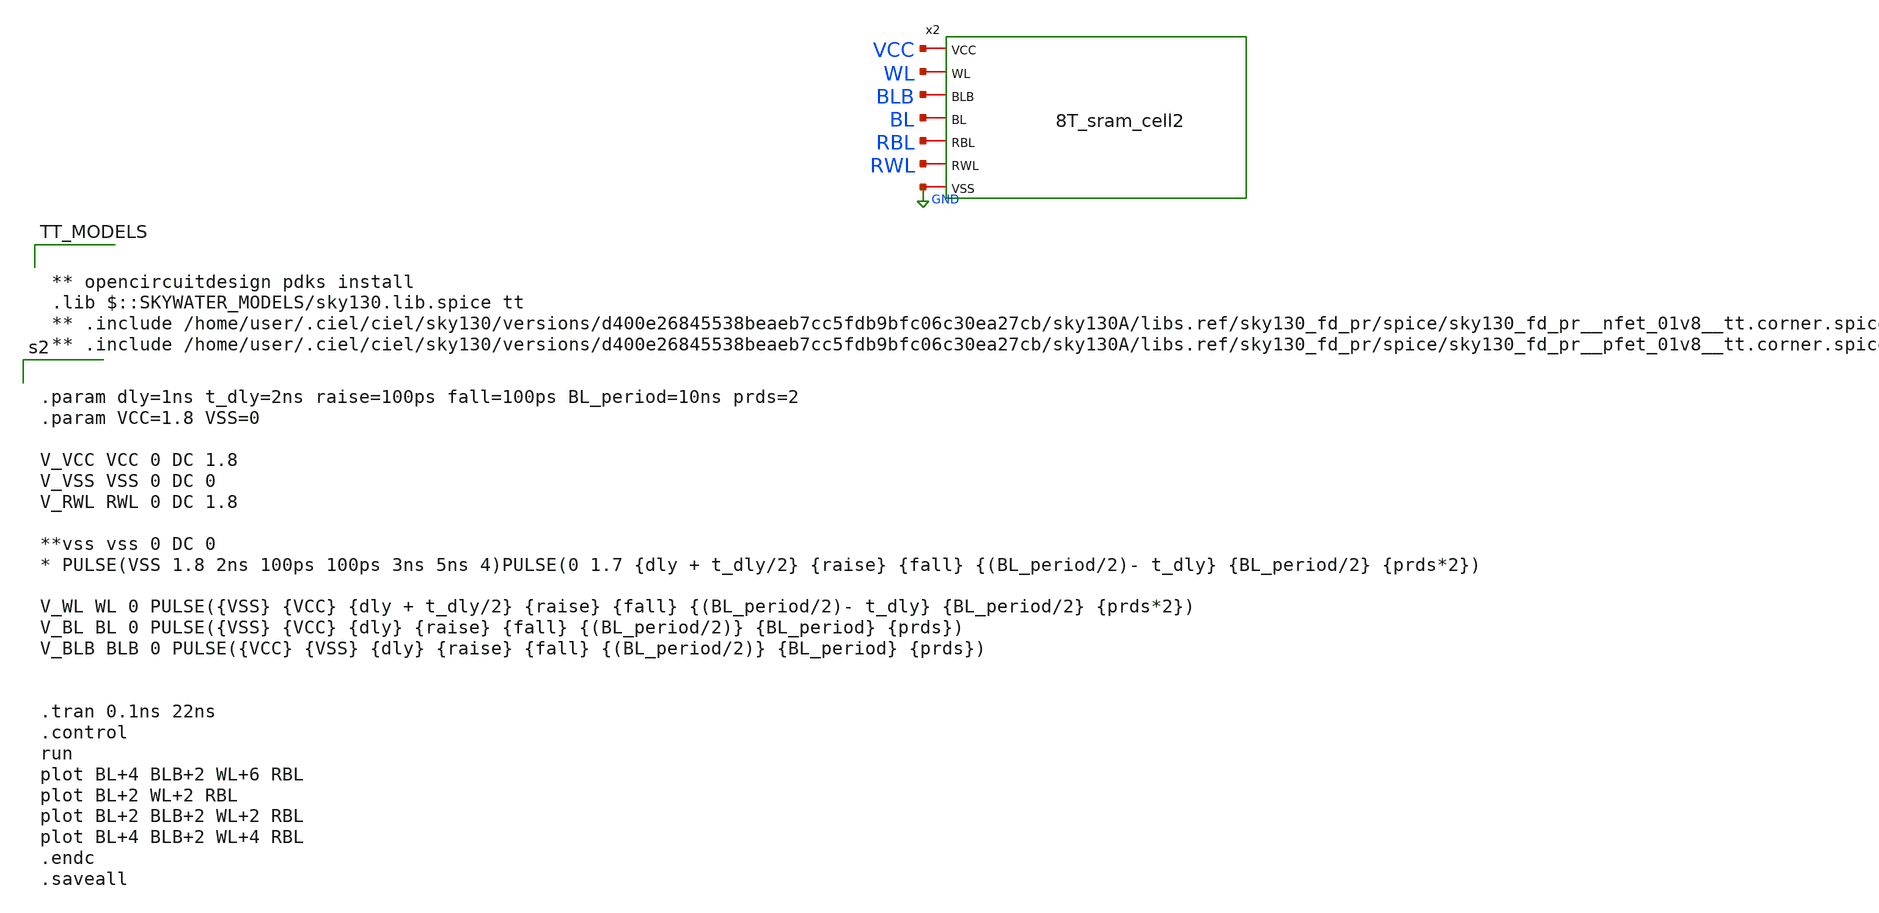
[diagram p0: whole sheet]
** sch_path: 8T_sram_array_test.sch
**.subckt 8T_sram_array_test
x2 VCC WL BLB BL RBL RWL GND 8T_sram_cell2
**** begin user architecture code


.param dly=1ns t_dly=2ns raise=100ps fall=100ps BL_period=10ns prds=2
.param VCC=1.8 VSS=0

V_VCC VCC 0 DC 1.8
V_VSS VSS 0 DC 0
V_RWL RWL 0 DC 1.8

**vss vss 0 DC 0
* PULSE(VSS 1.8 2ns 100ps 100ps 3ns 5ns 4)PULSE(0 1.7 {dly + t_dly/2} {raise} {fall} {(BL_period/2)- t_dly}
*+ {BL_period/2} {prds*2})

V_WL WL 0 PULSE({VSS} {VCC} {dly + t_dly/2} {raise} {fall} {(BL_period/2)- t_dly} {BL_period/2} {prds*2})
V_BL BL 0 PULSE({VSS} {VCC} {dly} {raise} {fall} {(BL_period/2)} {BL_period} {prds})
V_BLB BLB 0 PULSE({VCC} {VSS} {dly} {raise} {fall} {(BL_period/2)} {BL_period} {prds})


.tran 0.1ns 22ns
.control
run
plot BL+4 BLB+2 WL+6 RBL
plot BL+2 WL+2 RBL
plot BL+2 BLB+2 WL+2 RBL
plot BL+4 BLB+2 WL+4 RBL
.endc
.saveall




** opencircuitdesign pdks install
.lib $::SKYWATER_MODELS/sky130.lib.spice tt
** .include
*+ /home/user/.ciel/ciel/sky130/versions/d400e26845538beaeb7cc5fdb9bfc06c30ea27cb/sky130A/libs.ref/sky130_fd_pr/spice/sky130_fd_pr__nfet_01v8__tt.corner.spice
** .include
*+ /home/user/.ciel/ciel/sky130/versions/d400e26845538beaeb7cc5fdb9bfc06c30ea27cb/sky130A/libs.ref/sky130_fd_pr/spice/sky130_fd_pr__pfet_01v8__tt.corner.spice

**** end user architecture code
**.ends

* expanding   symbol:  8T_sram_cell2.sym # of pins=7
** sym_path: 8T_sram_cell2.sym
** sch_path: 8T_sram_cell2.sch
.subckt 8T_sram_cell2 VCC WL BLB BL RBL RWL VSS
*.iopin VCC
*.iopin BLB
*.iopin WL
*.iopin BL
*.iopin VSS
*.iopin RBL
*.iopin RWL
XM1 q_bar q VSS VSS sky130_fd_pr__nfet_01v8 L=0.15 W=1 nf=1 ad='int((1 + 1)/2) * 1 / 1 * 0.29' as='int((1 + 2)/2) * 1 / 1 * 0.29'
+ pd='2*int((1 + 1)/2) * (1 / 1 + 0.29)' ps='2*int((1 + 2)/2) * (1 / 1 + 0.29)' nrd='0.29 / 1 ' nrs='0.29 / 1 '
+ sa=0 sb=0 sd=0 mult=1 m=1
XM2 q q_bar VSS VSS sky130_fd_pr__nfet_01v8 L=0.15 W=1 nf=1 ad='int((1 + 1)/2) * 1 / 1 * 0.29' as='int((1 + 2)/2) * 1 / 1 * 0.29'
+ pd='2*int((1 + 1)/2) * (1 / 1 + 0.29)' ps='2*int((1 + 2)/2) * (1 / 1 + 0.29)' nrd='0.29 / 1 ' nrs='0.29 / 1 '
+ sa=0 sb=0 sd=0 mult=1 m=1
XM3 q_bar q VCC VCC sky130_fd_pr__pfet_01v8 L=0.15 W=4 nf=1 ad='int((1 + 1)/2) * 4 / 1 * 0.29' as='int((1 + 2)/2) * 4 / 1 * 0.29'
+ pd='2*int((1 + 1)/2) * (4 / 1 + 0.29)' ps='2*int((1 + 2)/2) * (4 / 1 + 0.29)' nrd='0.29 / 4 ' nrs='0.29 / 4 '
+ sa=0 sb=0 sd=0 mult=1 m=1
XM4 q q_bar VCC VCC sky130_fd_pr__pfet_01v8 L=0.15 W=4 nf=1 ad='int((1 + 1)/2) * 4 / 1 * 0.29' as='int((1 + 2)/2) * 4 / 1 * 0.29'
+ pd='2*int((1 + 1)/2) * (4 / 1 + 0.29)' ps='2*int((1 + 2)/2) * (4 / 1 + 0.29)' nrd='0.29 / 4 ' nrs='0.29 / 4 '
+ sa=0 sb=0 sd=0 mult=1 m=1
XM5 BLB WL q_bar VSS sky130_fd_pr__nfet_01v8 L=0.15 W=1 nf=1 ad='int((1 + 1)/2) * 1 / 1 * 0.29' as='int((1 + 2)/2) * 1 / 1 * 0.29'
+ pd='2*int((1 + 1)/2) * (1 / 1 + 0.29)' ps='2*int((1 + 2)/2) * (1 / 1 + 0.29)' nrd='0.29 / 1 ' nrs='0.29 / 1 '
+ sa=0 sb=0 sd=0 mult=1 m=1
XM8 q WL BL VSS sky130_fd_pr__nfet_01v8 L=0.15 W=1 nf=1 ad='int((1 + 1)/2) * 1 / 1 * 0.29' as='int((1 + 2)/2) * 1 / 1 * 0.29'
+ pd='2*int((1 + 1)/2) * (1 / 1 + 0.29)' ps='2*int((1 + 2)/2) * (1 / 1 + 0.29)' nrd='0.29 / 1 ' nrs='0.29 / 1 '
+ sa=0 sb=0 sd=0 mult=1 m=1
XM6 RBL q_bar VSS VSS sky130_fd_pr__nfet_01v8 L=0.15 W=1 nf=1 ad='int((1 + 1)/2) * 1 / 1 * 0.29' as='int((1 + 2)/2) * 1 / 1 * 0.29'
+ pd='2*int((1 + 1)/2) * (1 / 1 + 0.29)' ps='2*int((1 + 2)/2) * (1 / 1 + 0.29)' nrd='0.29 / 1 ' nrs='0.29 / 1 '
+ sa=0 sb=0 sd=0 mult=1 m=1
XM7 RBL q_bar RWL RWL sky130_fd_pr__pfet_01v8 L=0.15 W=4 nf=1 ad='int((1 + 1)/2) * 4 / 1 * 0.29' as='int((1 + 2)/2) * 4 / 1 * 0.29'
+ pd='2*int((1 + 1)/2) * (4 / 1 + 0.29)' ps='2*int((1 + 2)/2) * (4 / 1 + 0.29)' nrd='0.29 / 4 ' nrs='0.29 / 4 '
+ sa=0 sb=0 sd=0 mult=1 m=1
.ends

.GLOBAL GND
.end
